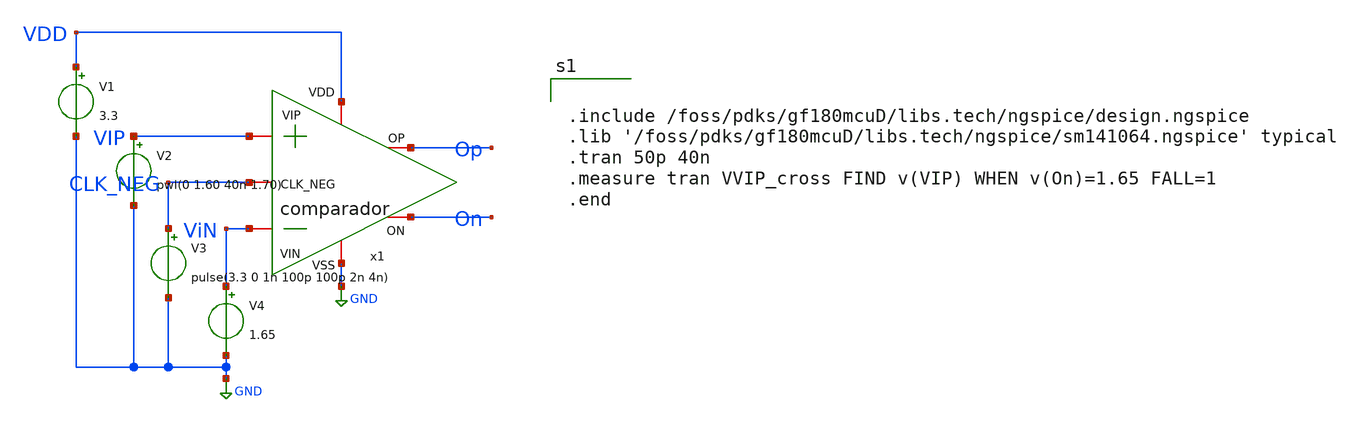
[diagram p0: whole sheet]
** sch_path: designs/sar_adc/comparator/comparador/xschem/tb_comparador_offset.sch
**.subckt tb_comparador_offset
V1 VDD GND 3.3
V2 VIP GND pwl(0 1.60 40n 1.70)
V3 CLK_NEG GND pulse(3.3 0 1n 100p 100p 2n 4n)
V4 ViN GND 1.65
x1 VDD CLK_NEG On Op ViN VIP GND comparador
**** begin user architecture code


.include /foss/pdks/gf180mcuD/libs.tech/ngspice/design.ngspice
.lib '/foss/pdks/gf180mcuD/libs.tech/ngspice/sm141064.ngspice' typical
.tran 50p 40n
.measure tran VVIP_cross FIND v(VIP) WHEN v(On)=1.65 FALL=1
.end


**** end user architecture code
**.ends

* expanding   symbol:  designs/sar_adc/comparator/comparador/xschem/comparador.sym # of pins=7
** sym_path: designs/sar_adc/comparator/comparador/xschem/comparador.sym
** sch_path: designs/sar_adc/comparator/comparador/xschem/comparador.sch
.subckt comparador VDD CLK_NEG ON OP VIN VIP VSS
*.iopin VSS
*.iopin VDD
*.iopin VIN
*.iopin VIP
*.iopin OP
*.iopin ON
*.iopin CLK_NEG
XM1 net3 CLK_NEG VDD VDD pfet_03v3 L=0.28u W=1.1u nf=1 ad='int((nf+1)/2) * W/nf * 0.18u' as='int((nf+2)/2) * W/nf * 0.18u'
+ pd='2*int((nf+1)/2) * (W/nf + 0.18u)' ps='2*int((nf+2)/2) * (W/nf + 0.18u)' nrd='0.18u / W' nrs='0.18u / W'
+ sa=0 sb=0 sd=0 m=1
XM2 AN CLK_NEG VSS VSS nfet_03v3 L=0.28u W=0.22u nf=1 ad='int((nf+1)/2) * W/nf * 0.18u' as='int((nf+2)/2) * W/nf * 0.18u'
+ pd='2*int((nf+1)/2) * (W/nf + 0.18u)' ps='2*int((nf+2)/2) * (W/nf + 0.18u)' nrd='0.18u / W' nrs='0.18u / W'
+ sa=0 sb=0 sd=0 m=1
XM3 AP VIP net3 VDD pfet_03v3 L=0.5u W=5u nf=1 ad='int((nf+1)/2) * W/nf * 0.18u' as='int((nf+2)/2) * W/nf * 0.18u'
+ pd='2*int((nf+1)/2) * (W/nf + 0.18u)' ps='2*int((nf+2)/2) * (W/nf + 0.18u)' nrd='0.18u / W' nrs='0.18u / W'
+ sa=0 sb=0 sd=0 m=1
XM4 AN VIN net3 VDD pfet_03v3 L=0.5u W=5u nf=1 ad='int((nf+1)/2) * W/nf * 0.18u' as='int((nf+2)/2) * W/nf * 0.18u'
+ pd='2*int((nf+1)/2) * (W/nf + 0.18u)' ps='2*int((nf+2)/2) * (W/nf + 0.18u)' nrd='0.18u / W' nrs='0.18u / W'
+ sa=0 sb=0 sd=0 m=1
XM5 AP CLK_NEG VSS VSS nfet_03v3 L=0.28u W=0.22u nf=1 ad='int((nf+1)/2) * W/nf * 0.18u' as='int((nf+2)/2) * W/nf * 0.18u'
+ pd='2*int((nf+1)/2) * (W/nf + 0.18u)' ps='2*int((nf+2)/2) * (W/nf + 0.18u)' nrd='0.18u / W' nrs='0.18u / W'
+ sa=0 sb=0 sd=0 m=1
XM6 ON OP VDD VDD pfet_03v3 L=0.28u W=0.22u nf=1 ad='int((nf+1)/2) * W/nf * 0.18u' as='int((nf+2)/2) * W/nf * 0.18u'
+ pd='2*int((nf+1)/2) * (W/nf + 0.18u)' ps='2*int((nf+2)/2) * (W/nf + 0.18u)' nrd='0.18u / W' nrs='0.18u / W'
+ sa=0 sb=0 sd=0 m=1
XM7 OP ON VDD VDD pfet_03v3 L=0.28u W=0.22u nf=1 ad='int((nf+1)/2) * W/nf * 0.18u' as='int((nf+2)/2) * W/nf * 0.18u'
+ pd='2*int((nf+1)/2) * (W/nf + 0.18u)' ps='2*int((nf+2)/2) * (W/nf + 0.18u)' nrd='0.18u / W' nrs='0.18u / W'
+ sa=0 sb=0 sd=0 m=1
XM8 ON OP net1 VSS nfet_03v3 L=0.28u W=0.22u nf=1 ad='int((nf+1)/2) * W/nf * 0.18u' as='int((nf+2)/2) * W/nf * 0.18u'
+ pd='2*int((nf+1)/2) * (W/nf + 0.18u)' ps='2*int((nf+2)/2) * (W/nf + 0.18u)' nrd='0.18u / W' nrs='0.18u / W'
+ sa=0 sb=0 sd=0 m=1
XM9 OP ON net2 VSS nfet_03v3 L=0.28u W=0.22u nf=1 ad='int((nf+1)/2) * W/nf * 0.18u' as='int((nf+2)/2) * W/nf * 0.18u'
+ pd='2*int((nf+1)/2) * (W/nf + 0.18u)' ps='2*int((nf+2)/2) * (W/nf + 0.18u)' nrd='0.18u / W' nrs='0.18u / W'
+ sa=0 sb=0 sd=0 m=1
XM10 net1 AN VSS VSS nfet_03v3 L=0.28u W=0.22u nf=1 ad='int((nf+1)/2) * W/nf * 0.18u' as='int((nf+2)/2) * W/nf * 0.18u'
+ pd='2*int((nf+1)/2) * (W/nf + 0.18u)' ps='2*int((nf+2)/2) * (W/nf + 0.18u)' nrd='0.18u / W' nrs='0.18u / W'
+ sa=0 sb=0 sd=0 m=1
XM11 net2 AP VSS VSS nfet_03v3 L=0.28u W=0.22u nf=1 ad='int((nf+1)/2) * W/nf * 0.18u' as='int((nf+2)/2) * W/nf * 0.18u'
+ pd='2*int((nf+1)/2) * (W/nf + 0.18u)' ps='2*int((nf+2)/2) * (W/nf + 0.18u)' nrd='0.18u / W' nrs='0.18u / W'
+ sa=0 sb=0 sd=0 m=1
XM12 ON AN VDD VDD pfet_03v3 L=0.28u W=0.22u nf=1 ad='int((nf+1)/2) * W/nf * 0.18u' as='int((nf+2)/2) * W/nf * 0.18u'
+ pd='2*int((nf+1)/2) * (W/nf + 0.18u)' ps='2*int((nf+2)/2) * (W/nf + 0.18u)' nrd='0.18u / W' nrs='0.18u / W'
+ sa=0 sb=0 sd=0 m=1
XM13 OP AP VDD VDD pfet_03v3 L=0.28u W=0.22u nf=1 ad='int((nf+1)/2) * W/nf * 0.18u' as='int((nf+2)/2) * W/nf * 0.18u'
+ pd='2*int((nf+1)/2) * (W/nf + 0.18u)' ps='2*int((nf+2)/2) * (W/nf + 0.18u)' nrd='0.18u / W' nrs='0.18u / W'
+ sa=0 sb=0 sd=0 m=1
XM14 net1 AN VDD VDD pfet_03v3 L=0.28u W=0.22u nf=1 ad='int((nf+1)/2) * W/nf * 0.18u' as='int((nf+2)/2) * W/nf * 0.18u'
+ pd='2*int((nf+1)/2) * (W/nf + 0.18u)' ps='2*int((nf+2)/2) * (W/nf + 0.18u)' nrd='0.18u / W' nrs='0.18u / W'
+ sa=0 sb=0 sd=0 m=1
XM15 net2 AP VDD VDD pfet_03v3 L=0.28u W=0.22u nf=1 ad='int((nf+1)/2) * W/nf * 0.18u' as='int((nf+2)/2) * W/nf * 0.18u'
+ pd='2*int((nf+1)/2) * (W/nf + 0.18u)' ps='2*int((nf+2)/2) * (W/nf + 0.18u)' nrd='0.18u / W' nrs='0.18u / W'
+ sa=0 sb=0 sd=0 m=1
.ends

.GLOBAL GND
.end
